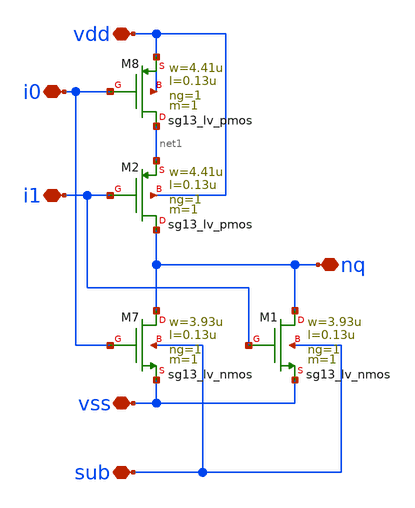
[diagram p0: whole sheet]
** sch_path: ihp-sg13cmos5l/libs.tech/xschem/hm_stdcells/sg13g2_io_nor2_x1_noptap.sch
**.subckt sg13g2_io_nor2_x1_noptap vss nq i0 vdd sub i1
*.iopin vss
*.iopin nq
*.iopin i0
*.iopin vdd
*.iopin sub
*.iopin i1
XM7 nq i0 vss sub sg13_lv_nmos w=3.93u l=0.13u ng=1 m=1 mm_ok=1
XM8 net1 i0 vdd vdd sg13_lv_pmos w=4.41u l=0.13u ng=1 m=1 mm_ok=1
XM1 nq i1 vss sub sg13_lv_nmos w=3.93u l=0.13u ng=1 m=1 mm_ok=1
XM2 nq i1 net1 vdd sg13_lv_pmos w=4.41u l=0.13u ng=1 m=1 mm_ok=1
**.ends
.end
